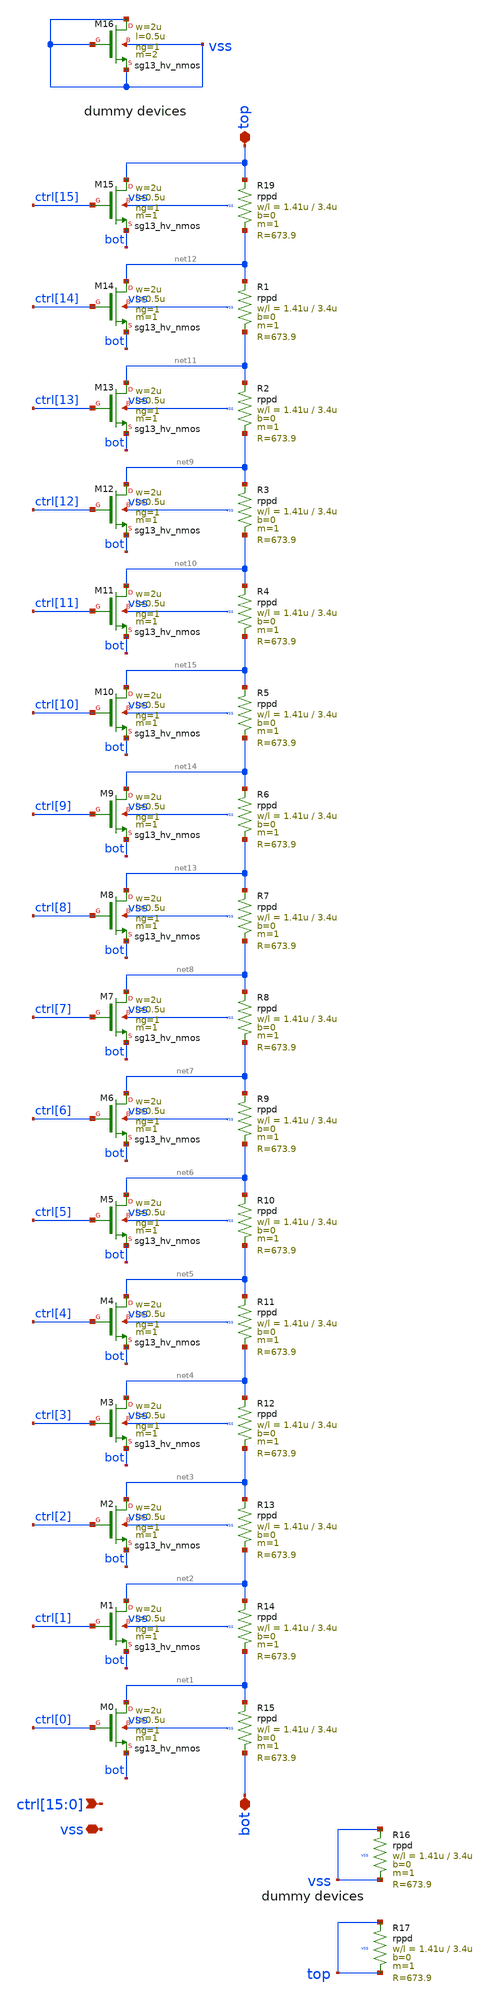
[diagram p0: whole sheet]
** sch_path: xschem/bg_trim.sch
**.subckt bg_trim vss
*+ ctrl[15],ctrl[14],ctrl[13],ctrl[12],ctrl[11],ctrl[10],ctrl[9],ctrl[8],ctrl[7],ctrl[6],ctrl[5],ctrl[4],ctrl[3],ctrl[2],ctrl[1],ctrl[0] bot top
*.iopin vss
*.ipin
*+ ctrl[15],ctrl[14],ctrl[13],ctrl[12],ctrl[11],ctrl[10],ctrl[9],ctrl[8],ctrl[7],ctrl[6],ctrl[5],ctrl[4],ctrl[3],ctrl[2],ctrl[1],ctrl[0]
*.iopin bot
*.iopin top
XM0 net1 ctrl[0] bot vss sg13_hv_nmos w=2u l=0.5u ng=1 m=1 mm_ok=1
XM1 net2 ctrl[1] bot vss sg13_hv_nmos w=2u l=0.5u ng=1 m=1 mm_ok=1
XM2 net3 ctrl[2] bot vss sg13_hv_nmos w=2u l=0.5u ng=1 m=1 mm_ok=1
XM3 net4 ctrl[3] bot vss sg13_hv_nmos w=2u l=0.5u ng=1 m=1 mm_ok=1
XM4 net5 ctrl[4] bot vss sg13_hv_nmos w=2u l=0.5u ng=1 m=1 mm_ok=1
XM5 net6 ctrl[5] bot vss sg13_hv_nmos w=2u l=0.5u ng=1 m=1 mm_ok=1
XM6 net7 ctrl[6] bot vss sg13_hv_nmos w=2u l=0.5u ng=1 m=1 mm_ok=1
XM7 net8 ctrl[7] bot vss sg13_hv_nmos w=2u l=0.5u ng=1 m=1 mm_ok=1
XM12 net9 ctrl[12] bot vss sg13_hv_nmos w=2u l=0.5u ng=1 m=1 mm_ok=1
XM13 net11 ctrl[13] bot vss sg13_hv_nmos w=2u l=0.5u ng=1 m=1 mm_ok=1
XM14 net12 ctrl[14] bot vss sg13_hv_nmos w=2u l=0.5u ng=1 m=1 mm_ok=1
XM15 top ctrl[15] bot vss sg13_hv_nmos w=2u l=0.5u ng=1 m=1 mm_ok=1
XM8 net13 ctrl[8] bot vss sg13_hv_nmos w=2u l=0.5u ng=1 m=1 mm_ok=1
XM9 net14 ctrl[9] bot vss sg13_hv_nmos w=2u l=0.5u ng=1 m=1 mm_ok=1
XM10 net15 ctrl[10] bot vss sg13_hv_nmos w=2u l=0.5u ng=1 m=1 mm_ok=1
XM11 net10 ctrl[11] bot vss sg13_hv_nmos w=2u l=0.5u ng=1 m=1 mm_ok=1
XM16 vss vss vss vss sg13_hv_nmos w=2u l=0.5u ng=1 m=2 mm_ok=1
XR19 top net12 vss rppd w=1.41u l=3.4u m=1 b=0 mm_ok=1
XR1 net12 net11 vss rppd w=1.41u l=3.4u m=1 b=0 mm_ok=1
XR2 net11 net9 vss rppd w=1.41u l=3.4u m=1 b=0 mm_ok=1
XR3 net9 net10 vss rppd w=1.41u l=3.4u m=1 b=0 mm_ok=1
XR4 net10 net15 vss rppd w=1.41u l=3.4u m=1 b=0 mm_ok=1
XR5 net15 net14 vss rppd w=1.41u l=3.4u m=1 b=0 mm_ok=1
XR6 net14 net13 vss rppd w=1.41u l=3.4u m=1 b=0 mm_ok=1
XR7 net13 net8 vss rppd w=1.41u l=3.4u m=1 b=0 mm_ok=1
XR8 net8 net7 vss rppd w=1.41u l=3.4u m=1 b=0 mm_ok=1
XR9 net7 net6 vss rppd w=1.41u l=3.4u m=1 b=0 mm_ok=1
XR10 net6 net5 vss rppd w=1.41u l=3.4u m=1 b=0 mm_ok=1
XR11 net5 net4 vss rppd w=1.41u l=3.4u m=1 b=0 mm_ok=1
XR12 net4 net3 vss rppd w=1.41u l=3.4u m=1 b=0 mm_ok=1
XR13 net3 net2 vss rppd w=1.41u l=3.4u m=1 b=0 mm_ok=1
XR14 net2 net1 vss rppd w=1.41u l=3.4u m=1 b=0 mm_ok=1
XR15 net1 bot vss rppd w=1.41u l=3.4u m=1 b=0 mm_ok=1
XR16 vss vss vss rppd w=1.41u l=3.4u m=1 b=0 mm_ok=1
XR17 top top vss rppd w=1.41u l=3.4u m=1 b=0 mm_ok=1
**.ends
.end
